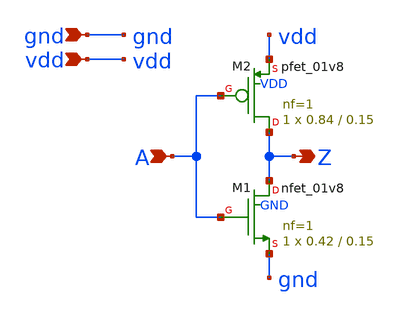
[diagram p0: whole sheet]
** sch_path: xschem/inv.sch
**.subckt inv A Z vdd gnd
*.ipin A
*.opin Z
*.ipin vdd
*.ipin gnd
XM1 Z A gnd GND sky130_fd_pr__nfet_01v8 L=0.15 W=0.42 nf=1 ad='int((nf+1)/2) * W/nf * 0.29' as='int((nf+2)/2) * W/nf * 0.29'
+ pd='2*int((nf+1)/2) * (W/nf + 0.29)' ps='2*int((nf+2)/2) * (W/nf + 0.29)' nrd='0.29 / W' nrs='0.29 / W'
+ sa=0 sb=0 sd=0 mult=1 m=1
XM2 Z A vdd VDD sky130_fd_pr__pfet_01v8 L=0.15 W=0.84 nf=1 ad='int((nf+1)/2) * W/nf * 0.29' as='int((nf+2)/2) * W/nf * 0.29'
+ pd='2*int((nf+1)/2) * (W/nf + 0.29)' ps='2*int((nf+2)/2) * (W/nf + 0.29)' nrd='0.29 / W' nrs='0.29 / W'
+ sa=0 sb=0 sd=0 mult=1 m=1
**.ends
.end
